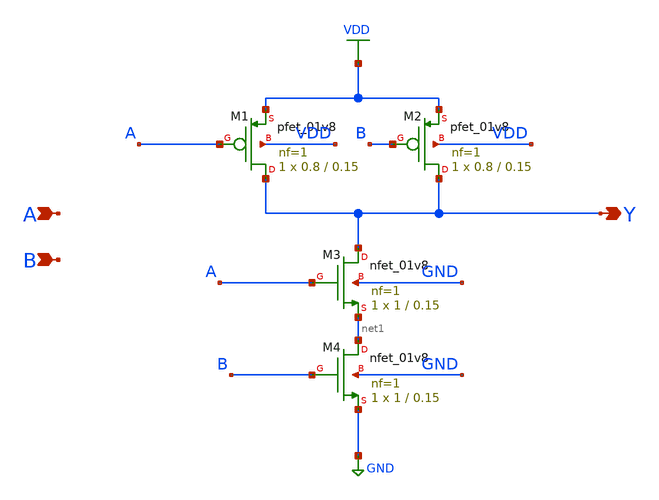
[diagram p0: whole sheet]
** sch_path: eng331lab_final/eng331lab_xschem/nand2.sch
**.subckt nand2 A B Y
*.ipin A
*.ipin B
*.opin Y
XM1 Y A VDD VDD sky130_fd_pr__pfet_01v8 L=0.15 W=0.8 nf=1 ad='int((1 + 1)/2) * 0.8 / 1 * 0.29' as='int((1 + 2)/2) * 0.8 / 1 * 0.29'
+ pd='2*int((1 + 1)/2) * (0.8 / 1 + 0.29)' ps='2*int((1 + 2)/2) * (0.8 / 1 + 0.29)' nrd='0.29 / 0.8 ' nrs='0.29 / 0.8 '
+ sa=0 sb=0 sd=0 mult=1 m=1
XM2 Y B VDD VDD sky130_fd_pr__pfet_01v8 L=0.15 W=0.8 nf=1 ad='int((1 + 1)/2) * 0.8 / 1 * 0.29' as='int((1 + 2)/2) * 0.8 / 1 * 0.29'
+ pd='2*int((1 + 1)/2) * (0.8 / 1 + 0.29)' ps='2*int((1 + 2)/2) * (0.8 / 1 + 0.29)' nrd='0.29 / 0.8 ' nrs='0.29 / 0.8 '
+ sa=0 sb=0 sd=0 mult=1 m=1
XM3 Y A net1 GND sky130_fd_pr__nfet_01v8 L=0.15 W=1 nf=1 ad='int((1 + 1)/2) * 1 / 1 * 0.29' as='int((1 + 2)/2) * 1 / 1 * 0.29'
+ pd='2*int((1 + 1)/2) * (1 / 1 + 0.29)' ps='2*int((1 + 2)/2) * (1 / 1 + 0.29)' nrd='0.29 / 1 ' nrs='0.29 / 1 '
+ sa=0 sb=0 sd=0 mult=1 m=1
XM4 net1 B GND GND sky130_fd_pr__nfet_01v8 L=0.15 W=1 nf=1 ad='int((1 + 1)/2) * 1 / 1 * 0.29' as='int((1 + 2)/2) * 1 / 1 * 0.29'
+ pd='2*int((1 + 1)/2) * (1 / 1 + 0.29)' ps='2*int((1 + 2)/2) * (1 / 1 + 0.29)' nrd='0.29 / 1 ' nrs='0.29 / 1 '
+ sa=0 sb=0 sd=0 mult=1 m=1
**.ends
.GLOBAL VDD
.GLOBAL GND
.end
